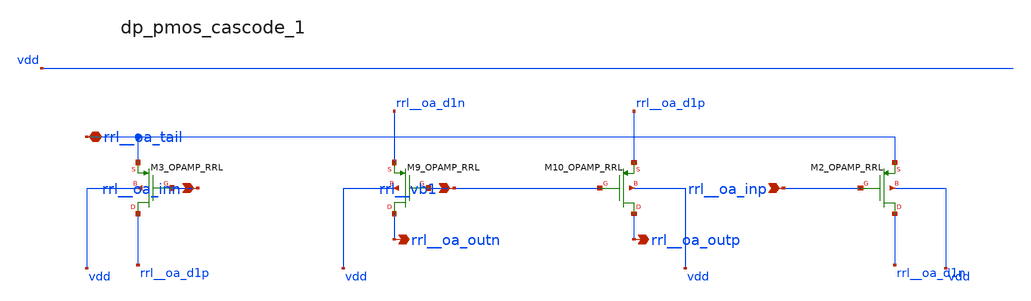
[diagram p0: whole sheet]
** sch_path: analog-db/raw/ia_004_fan_chopper_rrl/hier/blocks/dp_pmos_cascode_1.sch
**.subckt dp_pmos_cascode_1 rrl__oa_inn rrl__vb1 rrl__oa_inp rrl__oa_tail rrl__oa_outn rrl__oa_outp
*.ipin rrl__oa_inn
*.ipin rrl__vb1
*.ipin rrl__oa_inp
*.iopin rrl__oa_tail
*.opin rrl__oa_outn
*.opin rrl__oa_outp
XM10_OPAMP_RRL rrl__oa_outp rrl__vb1 rrl__oa_d1p vdd sg13_lv_pmos w=x_dut_xm10_opamp_rrl_w
+ l=x_dut_xm10_opamp_rrl_l ng=1 m=x_dut_xm10_opamp_rrl_m
XM2_OPAMP_RRL rrl__oa_d1n rrl__oa_inp rrl__oa_tail vdd sg13_lv_pmos w=x_dut_xm2_opamp_rrl_w
+ l=x_dut_xm2_opamp_rrl_l ng=1 m=x_dut_xm2_opamp_rrl_m
XM3_OPAMP_RRL rrl__oa_d1p rrl__oa_inn rrl__oa_tail vdd sg13_lv_pmos w=x_dut_xm3_opamp_rrl_w
+ l=x_dut_xm3_opamp_rrl_l ng=1 m=x_dut_xm3_opamp_rrl_m
XM9_OPAMP_RRL rrl__oa_outn rrl__vb1 rrl__oa_d1n vdd sg13_lv_pmos w=x_dut_xm9_opamp_rrl_w
+ l=x_dut_xm9_opamp_rrl_l ng=1 m=x_dut_xm9_opamp_rrl_m
**.ends
.end
